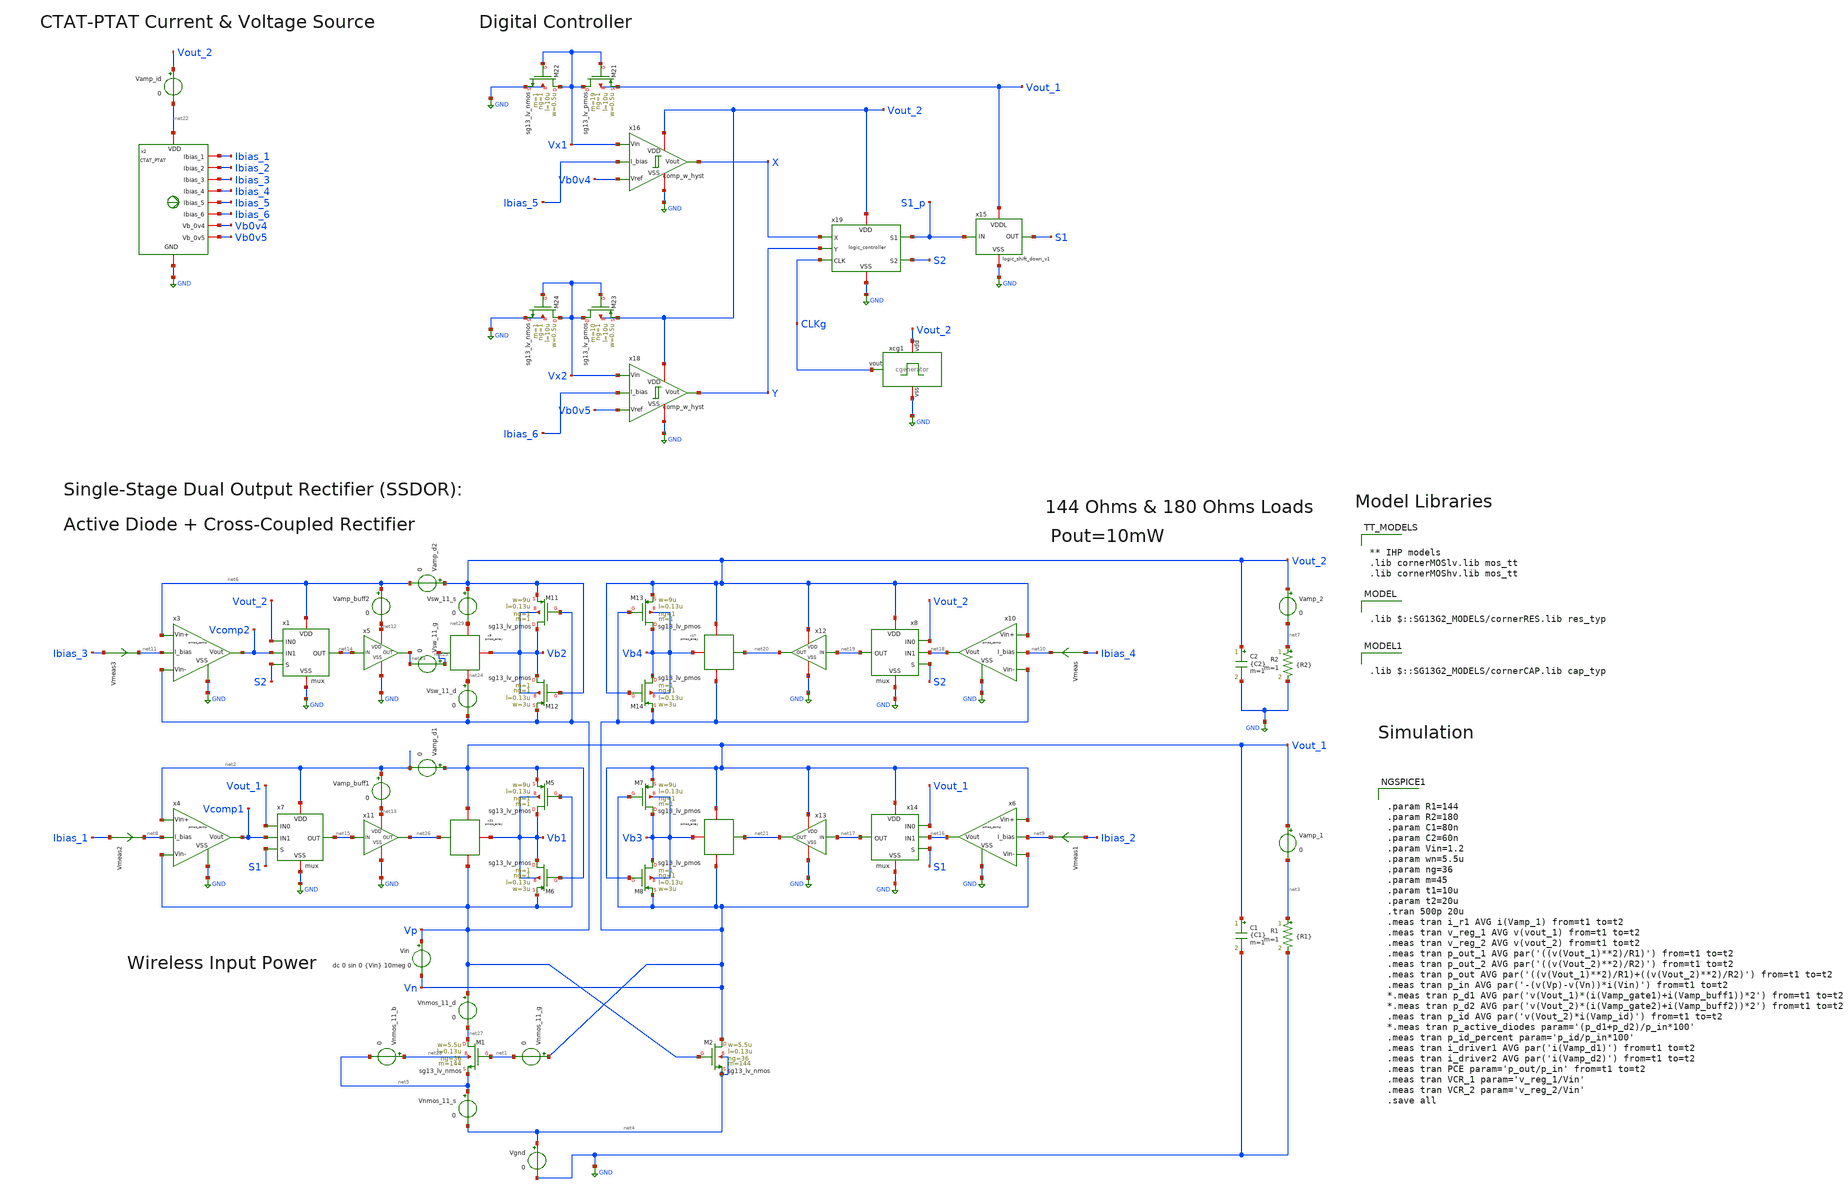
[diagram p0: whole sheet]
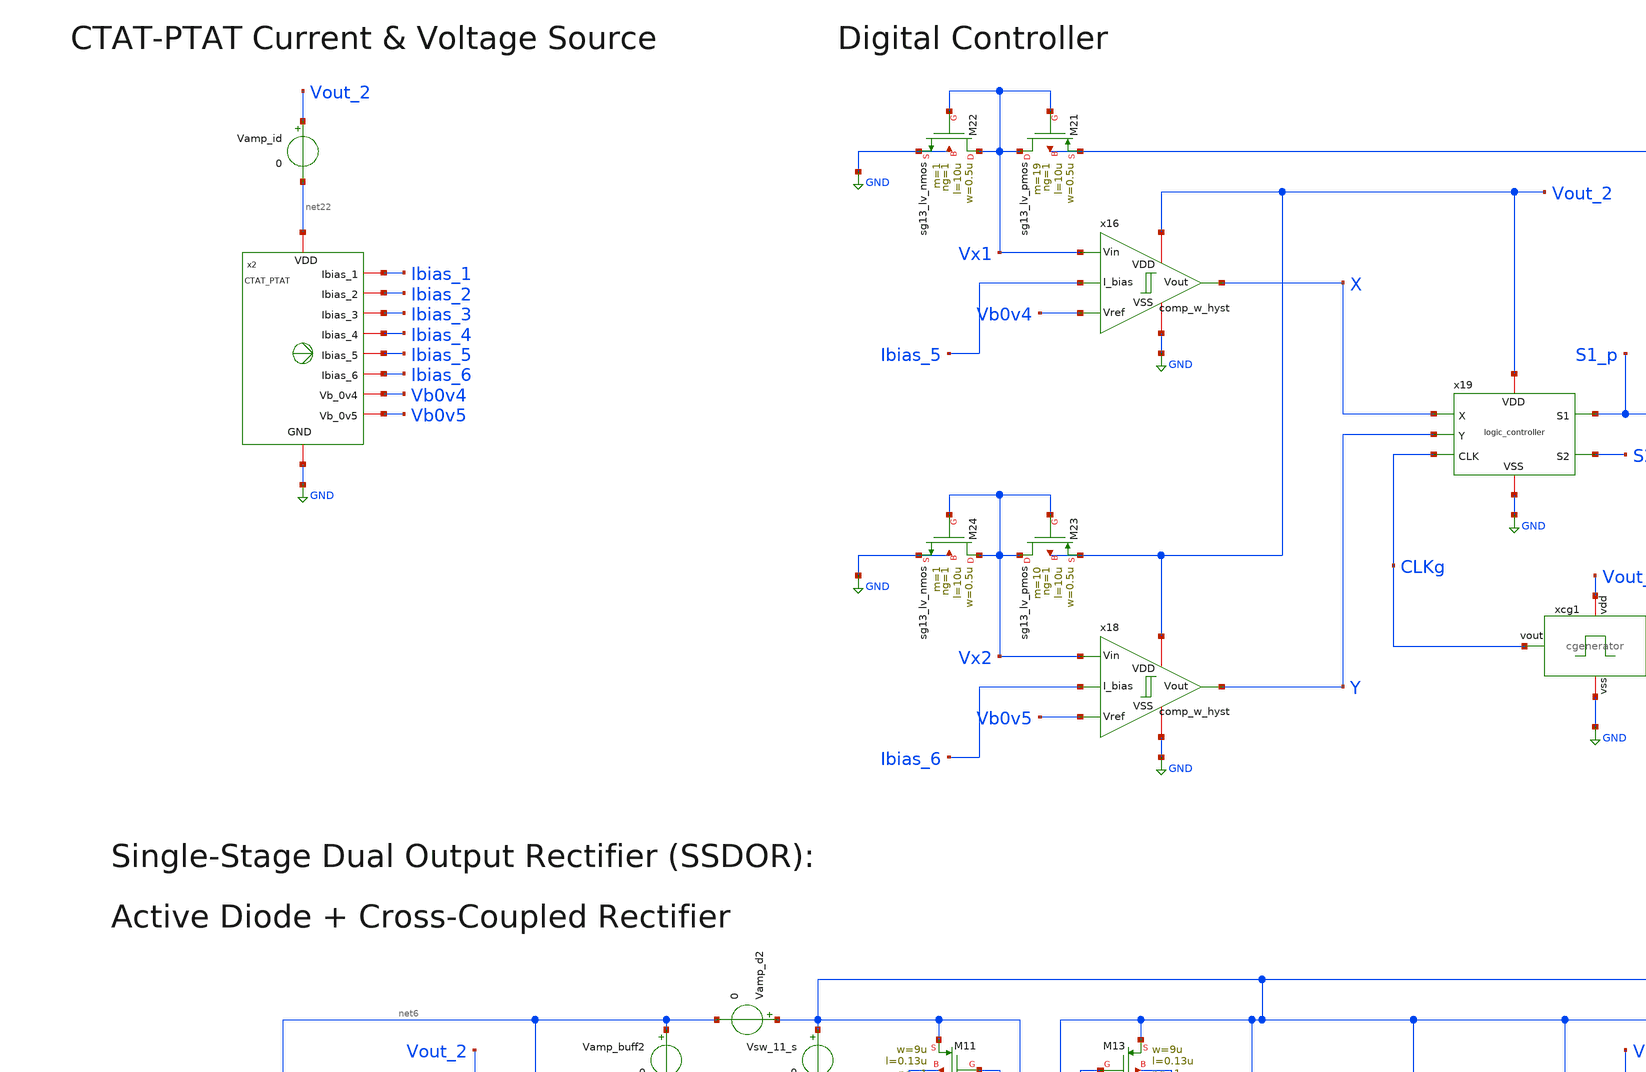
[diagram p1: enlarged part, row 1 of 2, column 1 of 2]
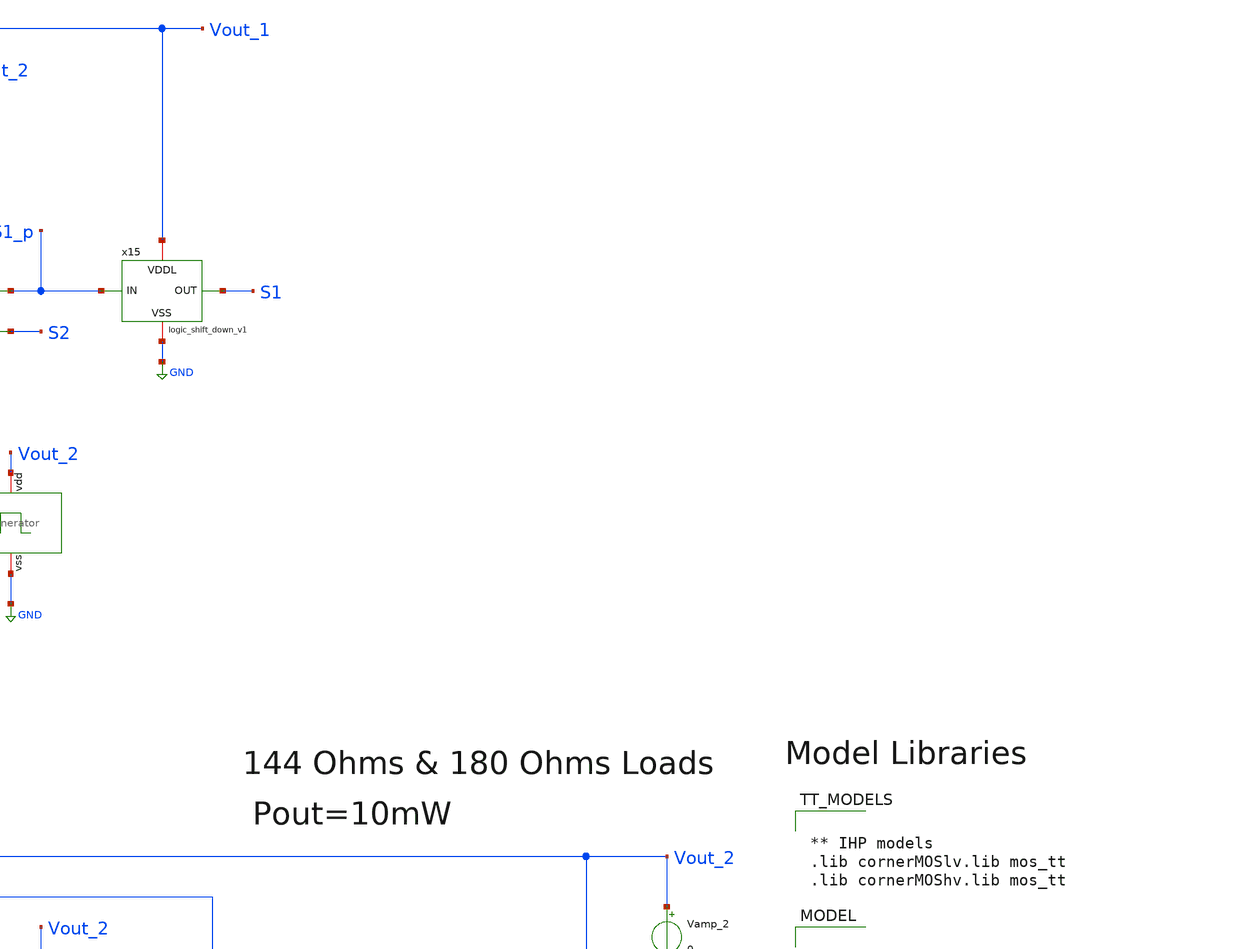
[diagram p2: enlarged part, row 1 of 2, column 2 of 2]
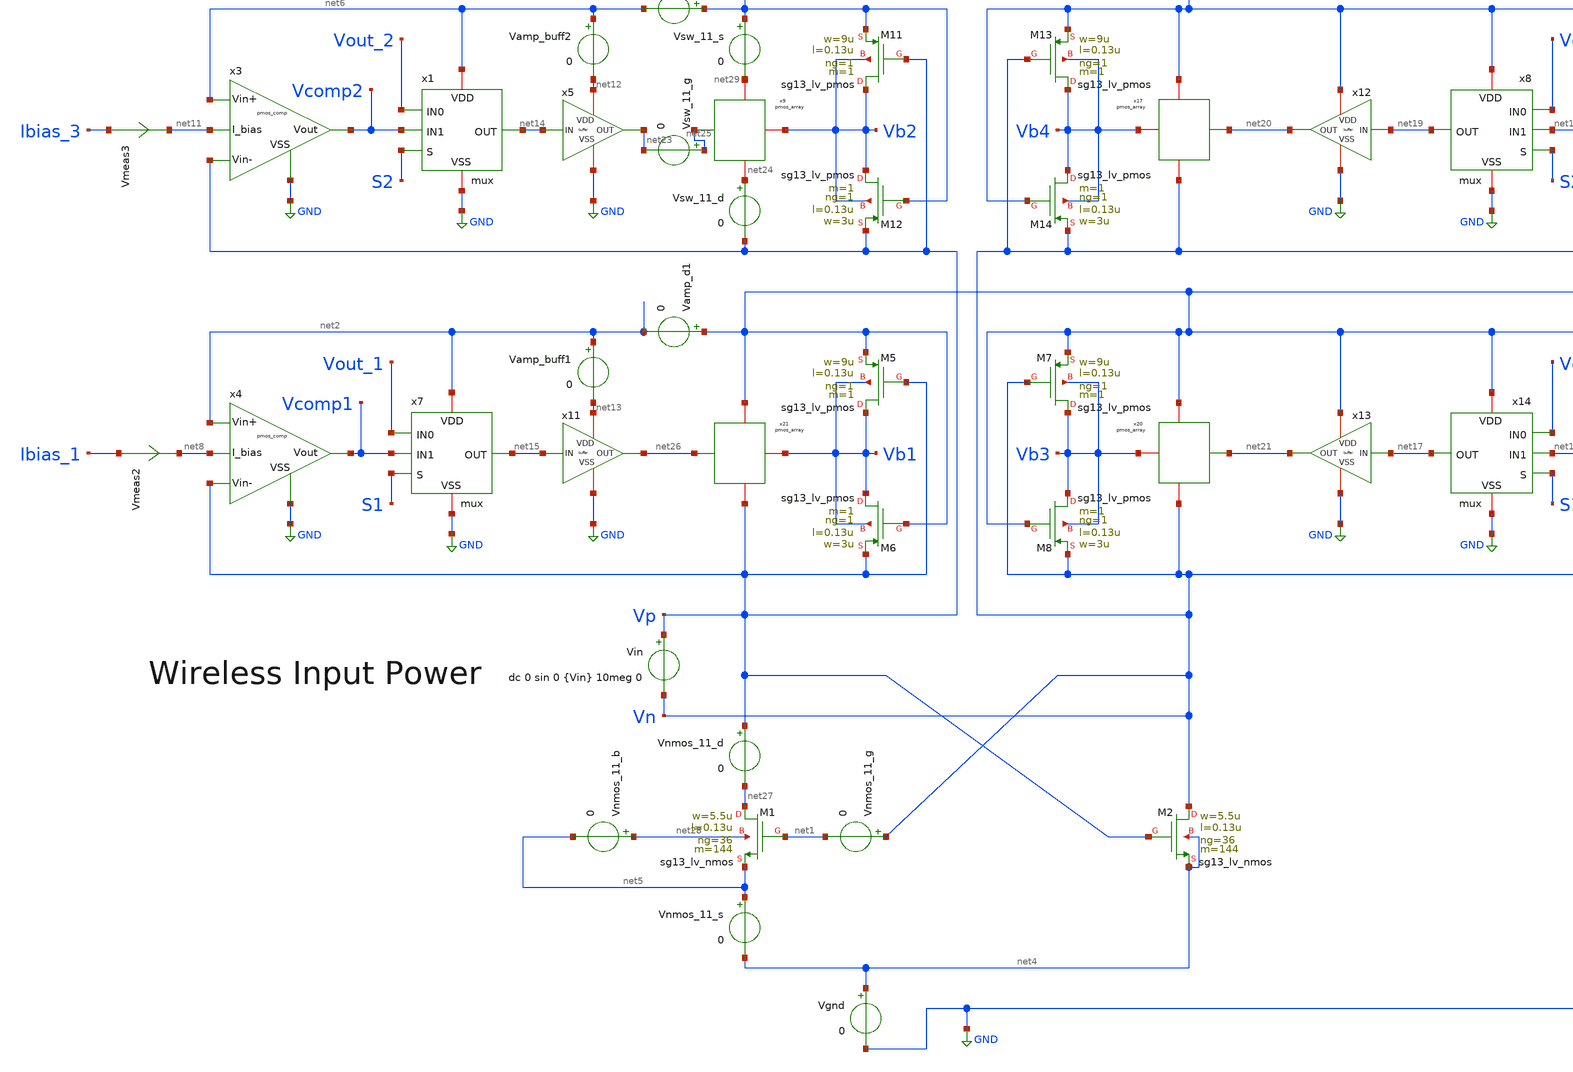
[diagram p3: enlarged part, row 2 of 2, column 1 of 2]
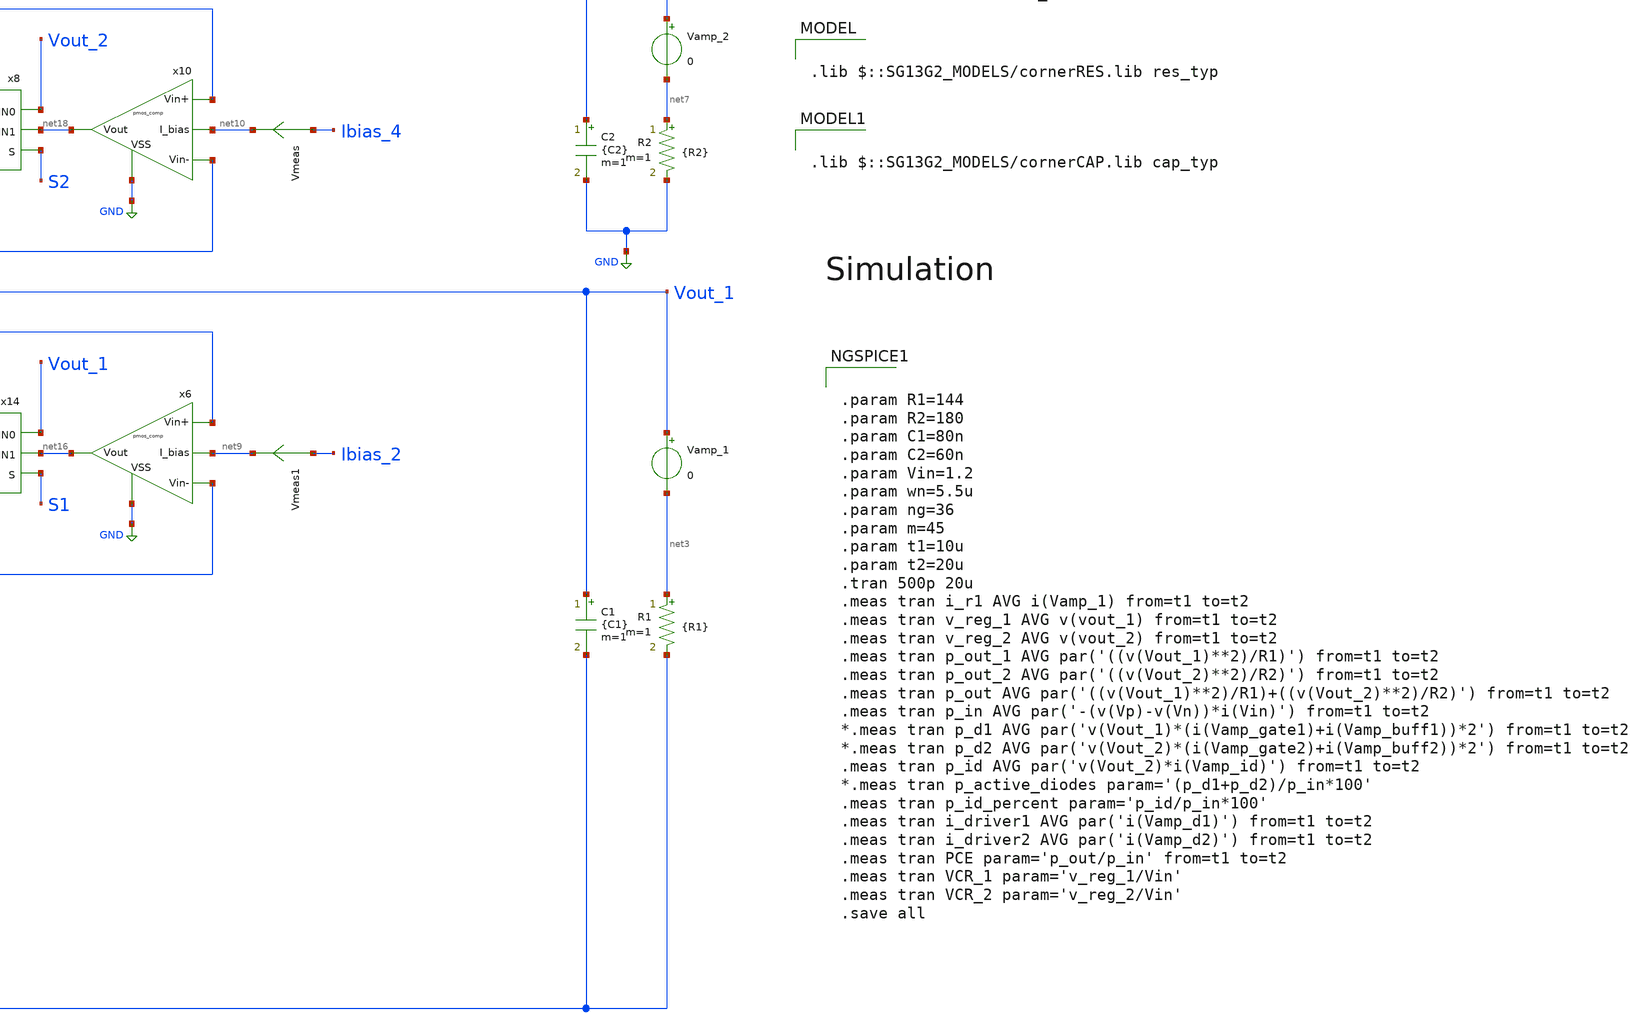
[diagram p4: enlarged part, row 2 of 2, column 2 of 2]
** sch_path: SSDOR_1.2V_v3/SSDOR_1.2V_v3_layout.sch
**.subckt SSDOR_1.2V_v3_layout
XM5 Vb1 Vp Vout_1 Vb1 sg13_lv_pmos w=9u l=0.13u ng=1 m=1 mm_ok=1
XM6 Vb1 Vout_1 Vp Vb1 sg13_lv_pmos w=3u l=0.13u ng=1 m=1 mm_ok=1
XM7 Vb3 Vn Vout_1 Vb3 sg13_lv_pmos w=9u l=0.13u ng=1 m=1 mm_ok=1
XM8 Vb3 Vout_1 Vn Vb3 sg13_lv_pmos w=3u l=0.13u ng=1 m=1 mm_ok=1
Vin Vp Vn dc 0 sin 0 {Vin} 10meg 0
C1 Vout_1 GND {C1} m=1
R1 net3 GND {R1} m=1
Vamp_1 Vout_1 net3 0
XM11 Vb2 Vp Vout_2 Vb2 sg13_lv_pmos w=9u l=0.13u ng=1 m=1 mm_ok=1
XM12 Vb2 Vout_2 Vp Vb2 sg13_lv_pmos w=3u l=0.13u ng=1 m=1 mm_ok=1
XM13 Vb4 Vn Vout_2 Vb4 sg13_lv_pmos w=9u l=0.13u ng=1 m=1 mm_ok=1
XM14 Vb4 Vout_2 Vn Vb4 sg13_lv_pmos w=3u l=0.13u ng=1 m=1 mm_ok=1
C2 Vout_2 GND {C2} m=1
R2 net7 GND {R2} m=1
Vamp_2 Vout_2 net7 0
XM21 Vx1 Vx1 Vout_1 Vout_1 sg13_lv_pmos w=0.5u l=10u ng=1 m=19 mm_ok=1
XM22 Vx1 Vx1 GND GND sg13_lv_nmos w=0.5u l=10u ng=1 m=1 mm_ok=1
XM23 Vx2 Vx2 Vout_2 Vout_2 sg13_lv_pmos w=0.5u l=10u ng=1 m=10 mm_ok=1
XM24 Vx2 Vx2 GND GND sg13_lv_nmos w=0.5u l=10u ng=1 m=1 mm_ok=1
Vamp_d2 Vout_2 net6 0
Vamp_d1 Vout_1 net2 0
Vamp_buff2 net6 net12 0
Vamp_buff1 net2 net13 0
Vmeas Ibias_4 net10 0
.save i(vmeas)
Vmeas1 Ibias_2 net9 0
.save i(vmeas1)
Vmeas2 Ibias_1 net8 0
.save i(vmeas2)
Vmeas3 Ibias_3 net11 0
.save i(vmeas3)
Vamp_id Vout_2 net22 0
x2 net22 GND Ibias_4 Ibias_1 Ibias_2 Ibias_5 Ibias_6 Ibias_3 Vb0v5 Vb0v4 CTAT_PTAT
x16 Vout_2 GND Vb0v4 Vx1 X Ibias_5 comp_w_hyst
x18 Vout_2 GND Vb0v5 Vx2 Y Ibias_6 comp_w_hyst
x19 Vout_2 X S1_p CLKg Y S2 GND logic_controller
x15 Vout_1 S1_p S1 GND logic_shift_down_v1
x3 Vp net6 Vcomp2 net11 GND pmos_comp
x4 Vp net2 Vcomp1 net8 GND pmos_comp
x6 Vn Vout_1 net16 net9 GND pmos_comp
x10 Vn Vout_2 net18 net10 GND pmos_comp
x1 net6 Vout_2 S2 net14 Vcomp2 GND mux
x7 net2 Vout_1 S1 net15 Vcomp1 GND mux
x8 Vout_2 Vout_2 S2 net19 net18 GND mux
x14 Vout_1 Vout_1 S1 net17 net16 GND mux
x5 net12 net14 net23 GND buffer wn=1u
x11 net13 net15 net26 GND buffer wn=1u
x12 Vout_2 net19 net20 GND buffer wn=1u
x13 Vout_1 net17 net21 GND buffer wn=1u
xcg1 Vout_2 CLKg GND cgenerator
Vsw_11_s Vout_2 net29 0
Vsw_11_g net25 net23 0
Vsw_11_d net24 Vp 0
x9 net29 net25 Vb2 net24 pmos_array
x17 Vout_2 net20 Vb4 Vn pmos_array
x20 Vout_1 net21 Vb3 Vn pmos_array
x21 Vout_1 net26 Vb1 Vp pmos_array
XM1 net27 net1 net5 net28 sg13_lv_nmos w=5.5u l=0.13u ng=36 m=144 mm_ok=1
XM2 Vn Vp net4 net4 sg13_lv_nmos w=5.5u l=0.13u ng=36 m=144 mm_ok=1
Vnmos_11_g Vn net1 0
Vnmos_11_d Vp net27 0
Vnmos_11_s net5 net4 0
Vnmos_11_b net28 net5 0
Vgnd net4 GND 0
**** begin user architecture code


** IHP models
.lib cornerMOSlv.lib mos_tt
.lib cornerMOShv.lib mos_tt



.lib $::SG13G2_MODELS/cornerRES.lib res_typ


.lib $::SG13G2_MODELS/cornerCAP.lib cap_typ



.param R1=144
.param R2=180
.param C1=80n
.param C2=60n
.param Vin=1.2
.param wn=5.5u
.param ng=36
.param m=45
.param t1=10u
.param t2=20u
.tran 500p 20u
.meas tran i_r1 AVG i(Vamp_1) from=t1 to=t2
.meas tran v_reg_1 AVG v(vout_1) from=t1 to=t2
.meas tran v_reg_2 AVG v(vout_2) from=t1 to=t2
.meas tran p_out_1 AVG par('((v(Vout_1)**2)/R1)') from=t1 to=t2
.meas tran p_out_2 AVG par('((v(Vout_2)**2)/R2)') from=t1 to=t2
.meas tran p_out AVG par('((v(Vout_1)**2)/R1)+((v(Vout_2)**2)/R2)') from=t1 to=t2
.meas tran p_in AVG par('-(v(Vp)-v(Vn))*i(Vin)') from=t1 to=t2
*.meas tran p_d1 AVG par('v(Vout_1)*(i(Vamp_gate1)+i(Vamp_buff1))*2') from=t1 to=t2
*.meas tran p_d2 AVG par('v(Vout_2)*(i(Vamp_gate2)+i(Vamp_buff2))*2') from=t1 to=t2
.meas tran p_id AVG par('v(Vout_2)*i(Vamp_id)') from=t1 to=t2
*.meas tran p_active_diodes param='(p_d1+p_d2)/p_in*100'
.meas tran p_id_percent param='p_id/p_in*100'
.meas tran i_driver1 AVG par('i(Vamp_d1)') from=t1 to=t2
.meas tran i_driver2 AVG par('i(Vamp_d2)') from=t1 to=t2
.meas tran PCE param='p_out/p_in' from=t1 to=t2
.meas tran VCR_1 param='v_reg_1/Vin'
.meas tran VCR_2 param='v_reg_2/Vin'
.save all


**** end user architecture code
**.ends
.GLOBAL GND
.end
